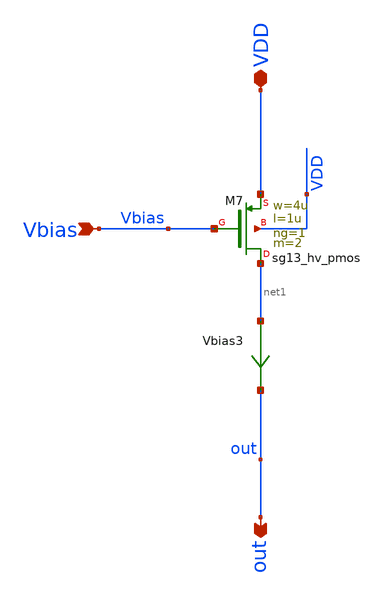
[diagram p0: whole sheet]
** sch_path: xschem/V2I/Idc.sch
**.subckt Idc VDD Vbias out
*.iopin VDD
*.ipin Vbias
*.opin out
XM7 net1 Vbias VDD VDD sg13_hv_pmos w=4u l=1u ng=1 m=2 mm_ok=1
Vbias3 net1 out 0
.save i(vbias3)
**.ends
.end
